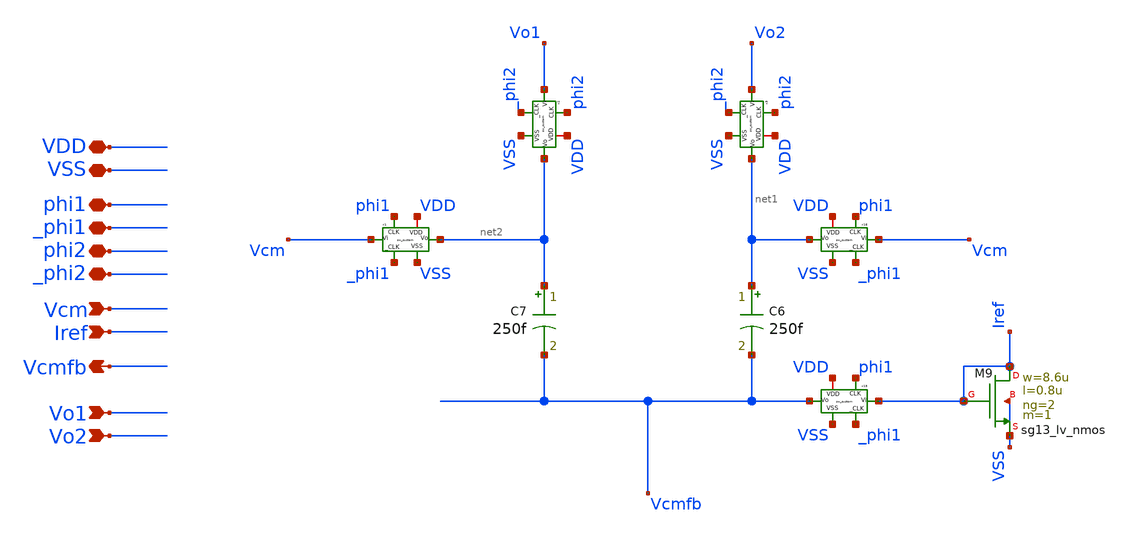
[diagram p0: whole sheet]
** sch_path: sch/blocks/cmfb.sch
**.subckt cmfb VDD VSS phi1 _phi1 phi2 _phi2 Vcm Iref Vcmfb Vo1 Vo2
*.iopin VDD
*.iopin VSS
*.iopin phi1
*.iopin _phi1
*.iopin phi2
*.iopin _phi2
*.ipin Vcm
*.ipin Iref
*.opin Vcmfb
*.ipin Vo1
*.ipin Vo2
x15 phi1 VSS Vcmfb Iref VDD _phi1 sw_custom
C6 net1 Vcmfb 250f m=1
x16 phi1 VSS net1 Vcm VDD _phi1 sw_custom
C7 net2 Vcmfb 250f m=1
x1 phi1 VSS net2 Vcm VDD _phi1 sw_custom
x2 phi2 VSS net2 Vo1 VDD _phi2 sw_custom
x3 phi2 VSS net1 Vo2 VDD _phi2 sw_custom
XM9 Iref Iref VSS VSS sg13_lv_nmos w=8.6u l=0.8u ng=2 m=1 mm_ok=1
**.ends

* expanding   symbol:  sw_custom.sym # of pins=6
** sym_path: sch/blocks/sw_custom.sym
** sch_path: sch/blocks/sw_custom.sch
.subckt sw_custom CLK VSS Vo Vi VDD _CLK
*.iopin VSS
*.ipin CLK
*.ipin _CLK
*.iopin Vi
*.iopin Vo
*.iopin VDD
S1 Vi Vo CLK VSS SW1
.ends

**** begin user architecture code
.MODEL SW1 SW   VT=0.9 VH=0.01  RON=0.01 ROFF=10G
**** end user architecture code
.end
